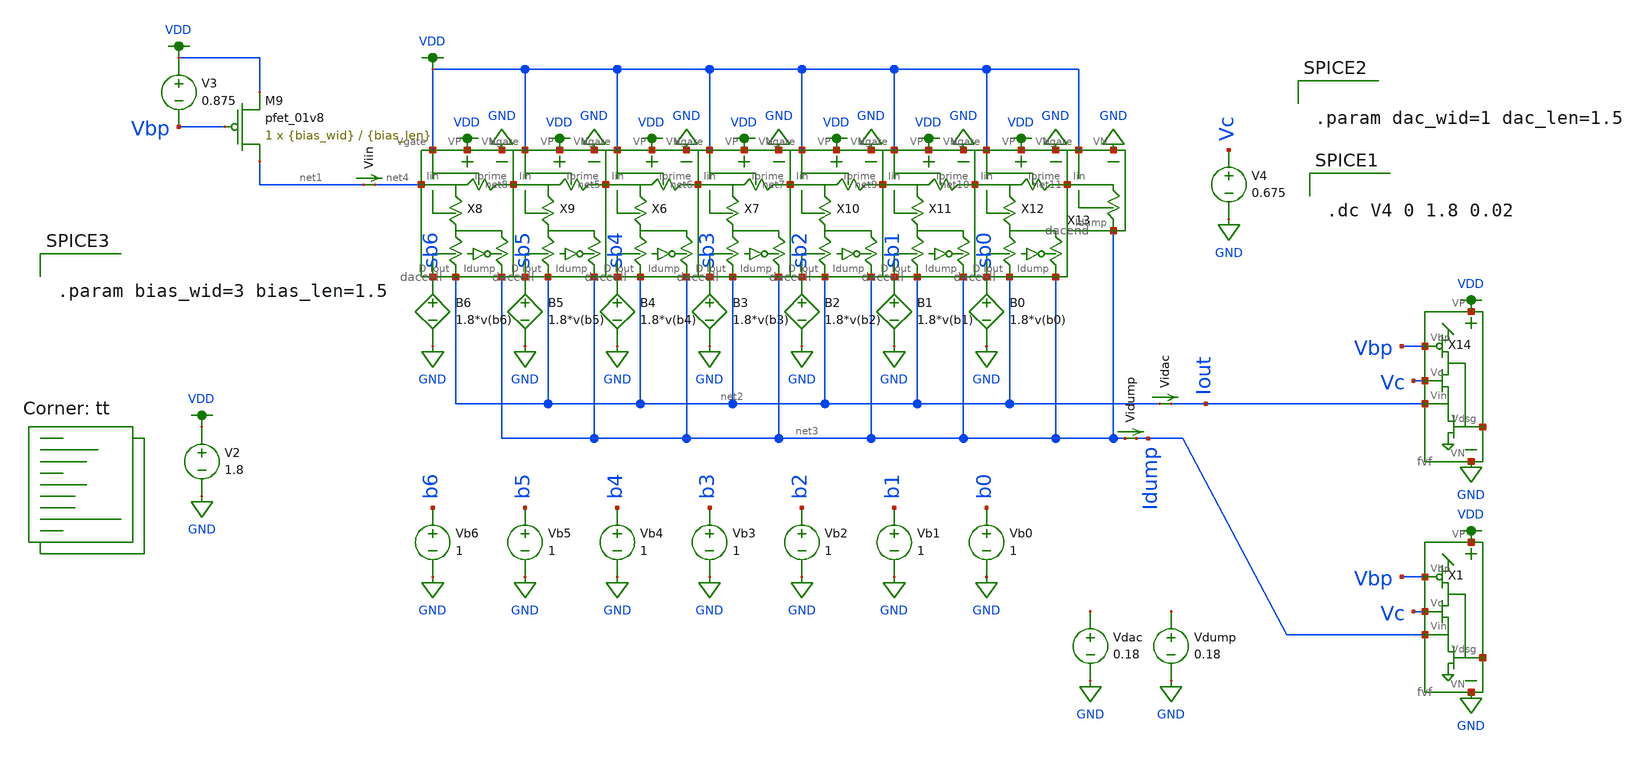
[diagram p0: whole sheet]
** sch_path: test_dac_3.sch
**.subckt test_dac_3
V2 VDD GND 1.8
X6 sb4 net3 VDD GND net2 net5 net6 VDD daccell
X7 sb3 net3 VDD GND net2 net6 net7 VDD daccell
X8 sb6 net3 VDD GND net2 net4 net8 VDD daccell
X9 sb5 net3 VDD GND net2 net8 net5 VDD daccell
X10 sb2 net3 VDD GND net2 net7 net9 VDD daccell
X11 sb1 net3 VDD GND net2 net9 net10 VDD daccell
X12 sb0 net3 VDD GND net2 net10 net11 VDD daccell
X13 net3 GND net11 VDD dacend
XM9 net1 Vbp VDD VP sky130_fd_pr__pfet_01v8 L={bias_len} W={bias_wid} nf=1 ad='int((nf+1)/2) * W/nf * 0.29'
+ as='int((nf+2)/2) * W/nf * 0.29' pd='2*int((nf+1)/2) * (W/nf + 0.29)' ps='2*int((nf+2)/2) * (W/nf + 0.29)'
+ nrd='0.29 / W' nrs='0.29 / W' sa=0 sb=0 sd=0 mult=1 m=1
Vb0 b0 GND 1
Viin net1 net4 0
.save i(viin)
B0 sb0 GND V=1.8*v(b0)
Vb1 b1 GND 1
B1 sb1 GND V=1.8*v(b1)
Vb2 b2 GND 1
B2 sb2 GND V=1.8*v(b2)
Vb3 b3 GND 1
B3 sb3 GND V=1.8*v(b3)
Vb4 b4 GND 1
B4 sb4 GND V=1.8*v(b4)
Vb5 b5 GND 1
B5 sb5 GND V=1.8*v(b5)
Vb6 b6 GND 1
B6 sb6 GND V=1.8*v(b6)
Vidump net3 Idump 0
.save i(vidump)
V3 VDD Vbp 0.875
Vidac net2 Iout 0
.save i(vidac)
Vdump net12 GND 0.18
Vdac net13 GND 0.18
X14 VDD Vbp Vc Iout net14 GND fvf
V4 Vc GND 0.675
X1 VDD Vbp Vc Idump net15 GND fvf
**** begin user architecture code
.lib $::SKYWATER_MODELS/sky130.lib.spice tt


.param dac_wid=1 dac_len=1.5




.param bias_wid=3 bias_len=1.5




.dc V4 0 1.8 0.02


**** end user architecture code
**.ends
.GLOBAL GND
.GLOBAL VDD
.end
